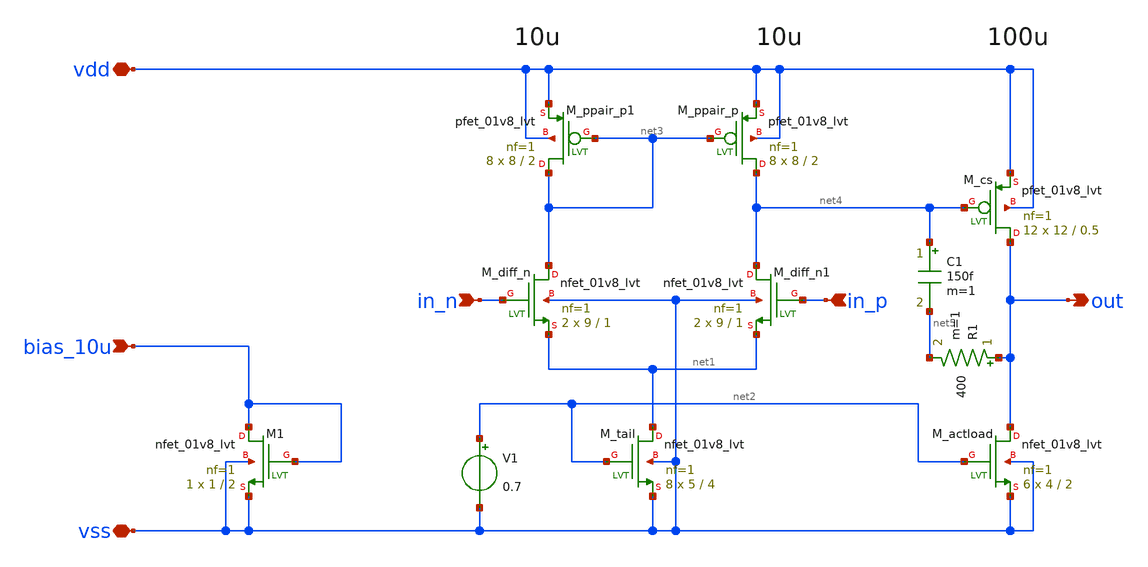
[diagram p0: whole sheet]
** sch_path: design/opamp/opamp.sch
**.subckt opamp vdd vss in_n in_p out bias_10u
*.iopin vdd
*.iopin vss
*.ipin in_n
*.ipin in_p
*.opin out
*.ipin bias_10u
XM1 bias_10u bias_10u vss vss sky130_fd_pr__nfet_01v8_lvt L=2 W=1 nf=1 ad='int((nf+1)/2) * W/nf * 0.29'
+ as='int((nf+2)/2) * W/nf * 0.29' pd='2*int((nf+1)/2) * (W/nf + 0.29)' ps='2*int((nf+2)/2) * (W/nf + 0.29)'
+ nrd='0.29 / W' nrs='0.29 / W' sa=0 sb=0 sd=0 mult=1 m=1
XM_diff_n net3 in_n net1 vss sky130_fd_pr__nfet_01v8_lvt L=1 W=9 nf=1 ad='int((nf+1)/2) * W/nf * 0.29'
+ as='int((nf+2)/2) * W/nf * 0.29' pd='2*int((nf+1)/2) * (W/nf + 0.29)' ps='2*int((nf+2)/2) * (W/nf + 0.29)'
+ nrd='0.29 / W' nrs='0.29 / W' sa=0 sb=0 sd=0 mult=2 m=2
XM_diff_n1 net4 in_p net1 vss sky130_fd_pr__nfet_01v8_lvt L=1 W=9 nf=1 ad='int((nf+1)/2) * W/nf * 0.29'
+ as='int((nf+2)/2) * W/nf * 0.29' pd='2*int((nf+1)/2) * (W/nf + 0.29)' ps='2*int((nf+2)/2) * (W/nf + 0.29)'
+ nrd='0.29 / W' nrs='0.29 / W' sa=0 sb=0 sd=0 mult=2 m=2
XM_tail net1 net2 vss vss sky130_fd_pr__nfet_01v8_lvt L=4 W=5 nf=1 ad='int((nf+1)/2) * W/nf * 0.29' as='int((nf+2)/2) * W/nf * 0.29'
+ pd='2*int((nf+1)/2) * (W/nf + 0.29)' ps='2*int((nf+2)/2) * (W/nf + 0.29)' nrd='0.29 / W' nrs='0.29 / W'
+ sa=0 sb=0 sd=0 mult=8 m=8
XM_actload out net2 vss vss sky130_fd_pr__nfet_01v8_lvt L=2 W=4 nf=1 ad='int((nf+1)/2) * W/nf * 0.29'
+ as='int((nf+2)/2) * W/nf * 0.29' pd='2*int((nf+1)/2) * (W/nf + 0.29)' ps='2*int((nf+2)/2) * (W/nf + 0.29)'
+ nrd='0.29 / W' nrs='0.29 / W' sa=0 sb=0 sd=0 mult=6 m=6
XM_ppair_p net4 net3 vdd vdd sky130_fd_pr__pfet_01v8_lvt L=2 W=8 nf=1 ad='int((nf+1)/2) * W/nf * 0.29'
+ as='int((nf+2)/2) * W/nf * 0.29' pd='2*int((nf+1)/2) * (W/nf + 0.29)' ps='2*int((nf+2)/2) * (W/nf + 0.29)'
+ nrd='0.29 / W' nrs='0.29 / W' sa=0 sb=0 sd=0 mult=8 m=8
XM_ppair_p1 net3 net3 vdd vdd sky130_fd_pr__pfet_01v8_lvt L=2 W=8 nf=1 ad='int((nf+1)/2) * W/nf * 0.29'
+ as='int((nf+2)/2) * W/nf * 0.29' pd='2*int((nf+1)/2) * (W/nf + 0.29)' ps='2*int((nf+2)/2) * (W/nf + 0.29)'
+ nrd='0.29 / W' nrs='0.29 / W' sa=0 sb=0 sd=0 mult=8 m=8
XM_cs out net4 vdd vdd sky130_fd_pr__pfet_01v8_lvt L=0.5 W=12 nf=1 ad='int((nf+1)/2) * W/nf * 0.29' as='int((nf+2)/2) * W/nf * 0.29'
+ pd='2*int((nf+1)/2) * (W/nf + 0.29)' ps='2*int((nf+2)/2) * (W/nf + 0.29)' nrd='0.29 / W' nrs='0.29 / W'
+ sa=0 sb=0 sd=0 mult=12 m=12
V1 net2 vss 0.7
C1 net4 net5 150f m=1
R1 out net5 400 m=1
**.ends
.end
